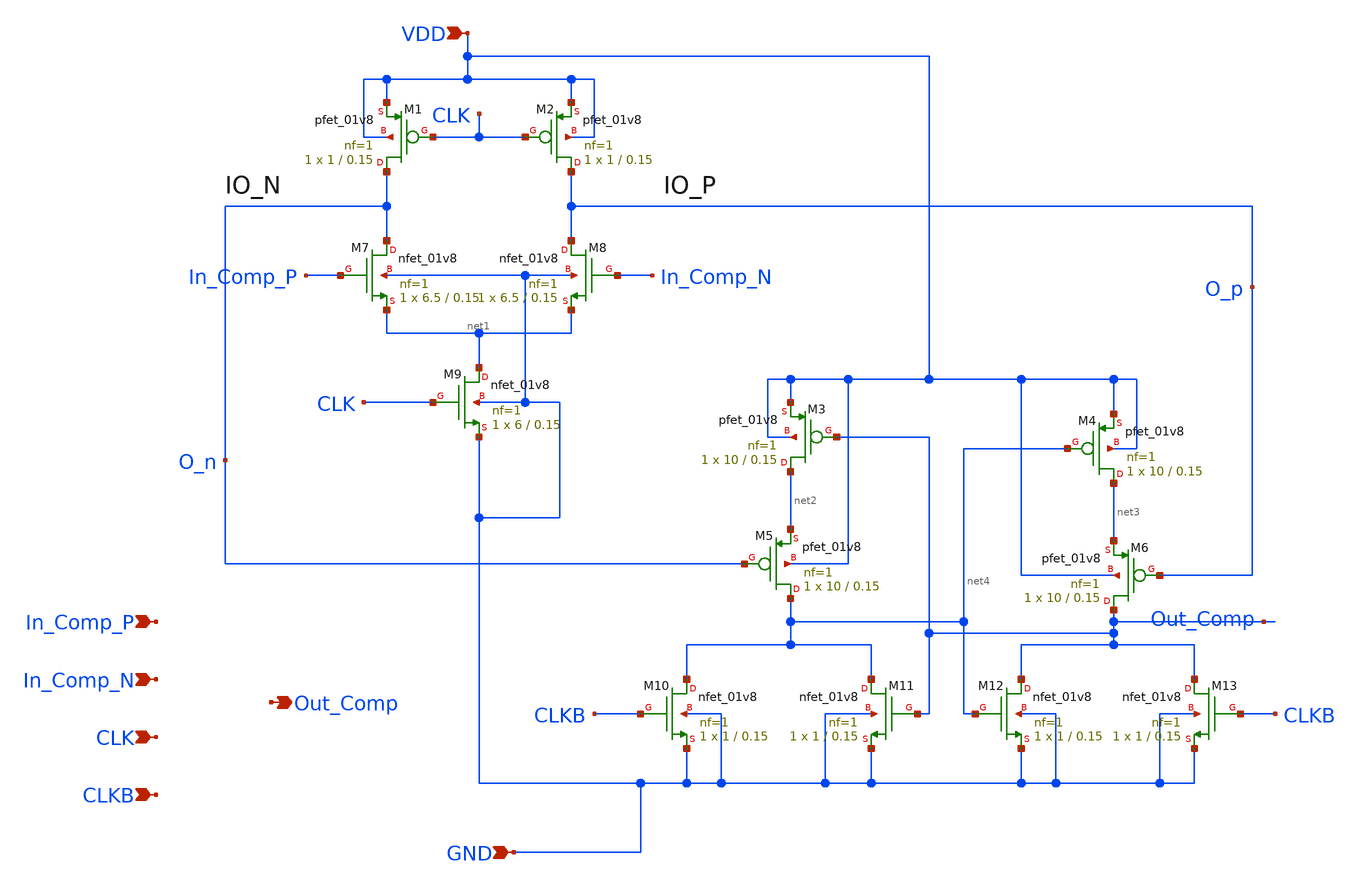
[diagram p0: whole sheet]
** sch_path: adc_comparator.sch
**.subckt adc_comparator VDD GND In_Comp_P In_Comp_N CLK CLKB Out_Comp
*.ipin VDD
*.ipin GND
*.ipin In_Comp_P
*.ipin In_Comp_N
*.ipin CLK
*.ipin CLKB
*.opin Out_Comp
XM1 O_n CLK VDD VDD sky130_fd_pr__pfet_01v8 L=0.15 W=1 nf=1 ad='int((nf+1)/2) * W/nf * 0.29' as='int((nf+2)/2) * W/nf * 0.29'
+ pd='2*int((nf+1)/2) * (W/nf + 0.29)' ps='2*int((nf+2)/2) * (W/nf + 0.29)' nrd='0.29 / W' nrs='0.29 / W'
+ sa=0 sb=0 sd=0 mult=1 m=1
XM2 O_p CLK VDD VDD sky130_fd_pr__pfet_01v8 L=0.15 W=1 nf=1 ad='int((nf+1)/2) * W/nf * 0.29' as='int((nf+2)/2) * W/nf * 0.29'
+ pd='2*int((nf+1)/2) * (W/nf + 0.29)' ps='2*int((nf+2)/2) * (W/nf + 0.29)' nrd='0.29 / W' nrs='0.29 / W'
+ sa=0 sb=0 sd=0 mult=1 m=1
XM3 net2 Out_Comp VDD VDD sky130_fd_pr__pfet_01v8 L=0.15 W=10 nf=1 ad='int((nf+1)/2) * W/nf * 0.29' as='int((nf+2)/2) * W/nf * 0.29'
+ pd='2*int((nf+1)/2) * (W/nf + 0.29)' ps='2*int((nf+2)/2) * (W/nf + 0.29)' nrd='0.29 / W' nrs='0.29 / W'
+ sa=0 sb=0 sd=0 mult=1 m=1
XM4 net3 net4 VDD VDD sky130_fd_pr__pfet_01v8 L=0.15 W=10 nf=1 ad='int((nf+1)/2) * W/nf * 0.29' as='int((nf+2)/2) * W/nf * 0.29'
+ pd='2*int((nf+1)/2) * (W/nf + 0.29)' ps='2*int((nf+2)/2) * (W/nf + 0.29)' nrd='0.29 / W' nrs='0.29 / W'
+ sa=0 sb=0 sd=0 mult=1 m=1
XM5 net4 O_n net2 VDD sky130_fd_pr__pfet_01v8 L=0.15 W=10 nf=1 ad='int((nf+1)/2) * W/nf * 0.29' as='int((nf+2)/2) * W/nf * 0.29'
+ pd='2*int((nf+1)/2) * (W/nf + 0.29)' ps='2*int((nf+2)/2) * (W/nf + 0.29)' nrd='0.29 / W' nrs='0.29 / W'
+ sa=0 sb=0 sd=0 mult=1 m=1
XM6 Out_Comp O_p net3 VDD sky130_fd_pr__pfet_01v8 L=0.15 W=10 nf=1 ad='int((nf+1)/2) * W/nf * 0.29' as='int((nf+2)/2) * W/nf * 0.29'
+ pd='2*int((nf+1)/2) * (W/nf + 0.29)' ps='2*int((nf+2)/2) * (W/nf + 0.29)' nrd='0.29 / W' nrs='0.29 / W'
+ sa=0 sb=0 sd=0 mult=1 m=1
XM7 O_n In_Comp_P net1 GND sky130_fd_pr__nfet_01v8 L=0.15 W=6.5 nf=1 ad='int((nf+1)/2) * W/nf * 0.29'
+ as='int((nf+2)/2) * W/nf * 0.29' pd='2*int((nf+1)/2) * (W/nf + 0.29)' ps='2*int((nf+2)/2) * (W/nf + 0.29)'
+ nrd='0.29 / W' nrs='0.29 / W' sa=0 sb=0 sd=0 mult=1 m=1
XM8 O_p In_Comp_N net1 GND sky130_fd_pr__nfet_01v8 L=0.15 W=6.5 nf=1 ad='int((nf+1)/2) * W/nf * 0.29'
+ as='int((nf+2)/2) * W/nf * 0.29' pd='2*int((nf+1)/2) * (W/nf + 0.29)' ps='2*int((nf+2)/2) * (W/nf + 0.29)'
+ nrd='0.29 / W' nrs='0.29 / W' sa=0 sb=0 sd=0 mult=1 m=1
XM9 net1 CLK GND GND sky130_fd_pr__nfet_01v8 L=0.15 W=6 nf=1 ad='int((nf+1)/2) * W/nf * 0.29' as='int((nf+2)/2) * W/nf * 0.29'
+ pd='2*int((nf+1)/2) * (W/nf + 0.29)' ps='2*int((nf+2)/2) * (W/nf + 0.29)' nrd='0.29 / W' nrs='0.29 / W'
+ sa=0 sb=0 sd=0 mult=1 m=1
XM10 net4 CLKB GND GND sky130_fd_pr__nfet_01v8 L=0.15 W=1 nf=1 ad='int((nf+1)/2) * W/nf * 0.29' as='int((nf+2)/2) * W/nf * 0.29'
+ pd='2*int((nf+1)/2) * (W/nf + 0.29)' ps='2*int((nf+2)/2) * (W/nf + 0.29)' nrd='0.29 / W' nrs='0.29 / W'
+ sa=0 sb=0 sd=0 mult=1 m=1
XM11 net4 Out_Comp GND GND sky130_fd_pr__nfet_01v8 L=0.15 W=1 nf=1 ad='int((nf+1)/2) * W/nf * 0.29' as='int((nf+2)/2) * W/nf * 0.29'
+ pd='2*int((nf+1)/2) * (W/nf + 0.29)' ps='2*int((nf+2)/2) * (W/nf + 0.29)' nrd='0.29 / W' nrs='0.29 / W'
+ sa=0 sb=0 sd=0 mult=1 m=1
XM12 Out_Comp net4 GND GND sky130_fd_pr__nfet_01v8 L=0.15 W=1 nf=1 ad='int((nf+1)/2) * W/nf * 0.29' as='int((nf+2)/2) * W/nf * 0.29'
+ pd='2*int((nf+1)/2) * (W/nf + 0.29)' ps='2*int((nf+2)/2) * (W/nf + 0.29)' nrd='0.29 / W' nrs='0.29 / W'
+ sa=0 sb=0 sd=0 mult=1 m=1
XM13 Out_Comp CLKB GND GND sky130_fd_pr__nfet_01v8 L=0.15 W=1 nf=1 ad='int((nf+1)/2) * W/nf * 0.29' as='int((nf+2)/2) * W/nf * 0.29'
+ pd='2*int((nf+1)/2) * (W/nf + 0.29)' ps='2*int((nf+2)/2) * (W/nf + 0.29)' nrd='0.29 / W' nrs='0.29 / W'
+ sa=0 sb=0 sd=0 mult=1 m=1
**.ends
.end
